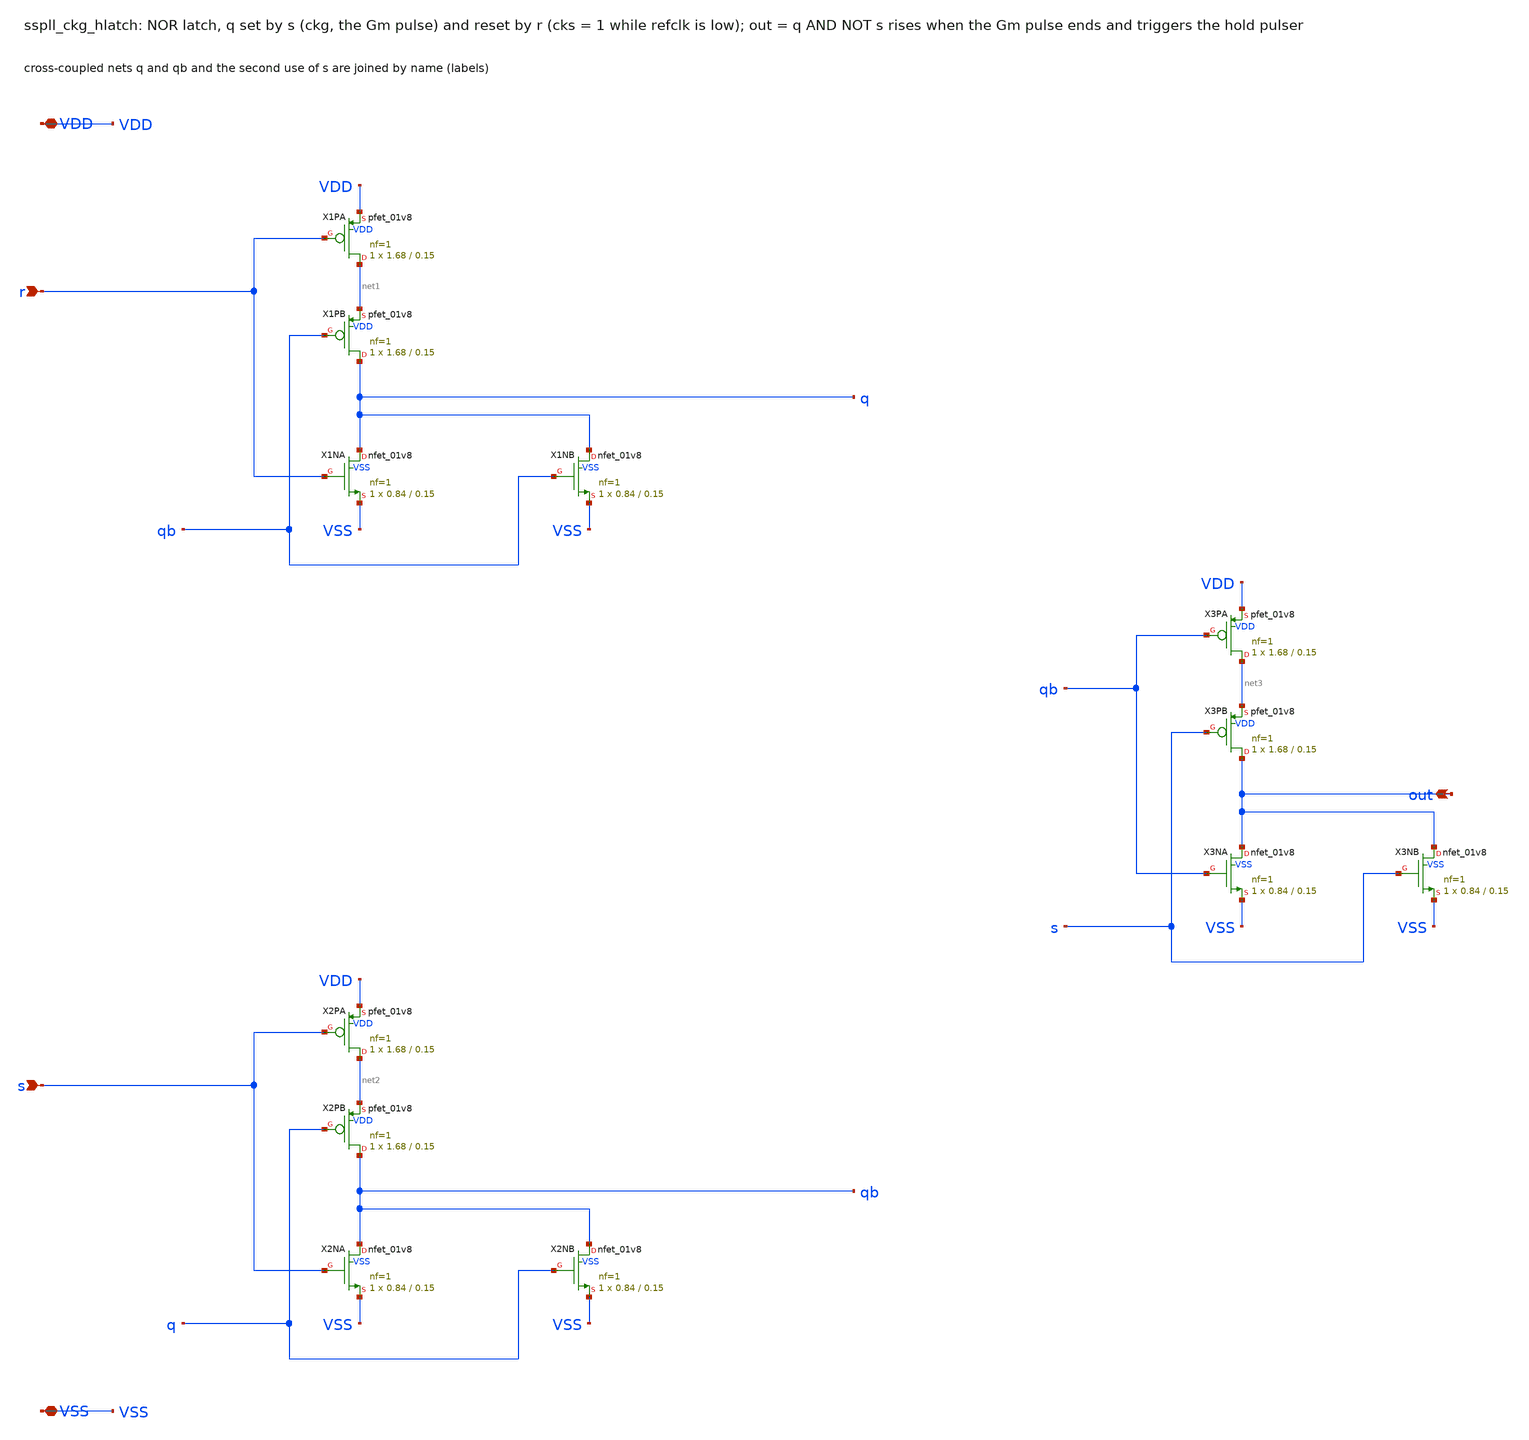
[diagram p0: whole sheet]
** sch_path: xschem/clkgen/sspll_ckg_hlatch.sch
**.subckt sspll_ckg_hlatch r s out VDD VSS
*.ipin r
*.ipin s
*.opin out
*.iopin VDD
*.iopin VSS
XX1PA net1 r VDD VDD sky130_fd_pr__pfet_01v8 L=0.15 W=1.68 nf=1 ad='int((nf+1)/2) * W/nf * 0.29' as='int((nf+2)/2) * W/nf * 0.29'
+ pd='2*int((nf+1)/2) * (W/nf + 0.29)' ps='2*int((nf+2)/2) * (W/nf + 0.29)' nrd='0.29 / W' nrs='0.29 / W'
+ sa=0 sb=0 sd=0 mult=1 m=1
XX1PB q qb net1 VDD sky130_fd_pr__pfet_01v8 L=0.15 W=1.68 nf=1 ad='int((nf+1)/2) * W/nf * 0.29' as='int((nf+2)/2) * W/nf * 0.29'
+ pd='2*int((nf+1)/2) * (W/nf + 0.29)' ps='2*int((nf+2)/2) * (W/nf + 0.29)' nrd='0.29 / W' nrs='0.29 / W'
+ sa=0 sb=0 sd=0 mult=1 m=1
XX1NA q r VSS VSS sky130_fd_pr__nfet_01v8 L=0.15 W=0.84 nf=1 ad='int((nf+1)/2) * W/nf * 0.29' as='int((nf+2)/2) * W/nf * 0.29'
+ pd='2*int((nf+1)/2) * (W/nf + 0.29)' ps='2*int((nf+2)/2) * (W/nf + 0.29)' nrd='0.29 / W' nrs='0.29 / W'
+ sa=0 sb=0 sd=0 mult=1 m=1
XX1NB q qb VSS VSS sky130_fd_pr__nfet_01v8 L=0.15 W=0.84 nf=1 ad='int((nf+1)/2) * W/nf * 0.29' as='int((nf+2)/2) * W/nf * 0.29'
+ pd='2*int((nf+1)/2) * (W/nf + 0.29)' ps='2*int((nf+2)/2) * (W/nf + 0.29)' nrd='0.29 / W' nrs='0.29 / W'
+ sa=0 sb=0 sd=0 mult=1 m=1
XX2PA net2 s VDD VDD sky130_fd_pr__pfet_01v8 L=0.15 W=1.68 nf=1 ad='int((nf+1)/2) * W/nf * 0.29' as='int((nf+2)/2) * W/nf * 0.29'
+ pd='2*int((nf+1)/2) * (W/nf + 0.29)' ps='2*int((nf+2)/2) * (W/nf + 0.29)' nrd='0.29 / W' nrs='0.29 / W'
+ sa=0 sb=0 sd=0 mult=1 m=1
XX2PB qb q net2 VDD sky130_fd_pr__pfet_01v8 L=0.15 W=1.68 nf=1 ad='int((nf+1)/2) * W/nf * 0.29' as='int((nf+2)/2) * W/nf * 0.29'
+ pd='2*int((nf+1)/2) * (W/nf + 0.29)' ps='2*int((nf+2)/2) * (W/nf + 0.29)' nrd='0.29 / W' nrs='0.29 / W'
+ sa=0 sb=0 sd=0 mult=1 m=1
XX2NA qb s VSS VSS sky130_fd_pr__nfet_01v8 L=0.15 W=0.84 nf=1 ad='int((nf+1)/2) * W/nf * 0.29' as='int((nf+2)/2) * W/nf * 0.29'
+ pd='2*int((nf+1)/2) * (W/nf + 0.29)' ps='2*int((nf+2)/2) * (W/nf + 0.29)' nrd='0.29 / W' nrs='0.29 / W'
+ sa=0 sb=0 sd=0 mult=1 m=1
XX2NB qb q VSS VSS sky130_fd_pr__nfet_01v8 L=0.15 W=0.84 nf=1 ad='int((nf+1)/2) * W/nf * 0.29' as='int((nf+2)/2) * W/nf * 0.29'
+ pd='2*int((nf+1)/2) * (W/nf + 0.29)' ps='2*int((nf+2)/2) * (W/nf + 0.29)' nrd='0.29 / W' nrs='0.29 / W'
+ sa=0 sb=0 sd=0 mult=1 m=1
XX3PA net3 qb VDD VDD sky130_fd_pr__pfet_01v8 L=0.15 W=1.68 nf=1 ad='int((nf+1)/2) * W/nf * 0.29' as='int((nf+2)/2) * W/nf * 0.29'
+ pd='2*int((nf+1)/2) * (W/nf + 0.29)' ps='2*int((nf+2)/2) * (W/nf + 0.29)' nrd='0.29 / W' nrs='0.29 / W'
+ sa=0 sb=0 sd=0 mult=1 m=1
XX3PB out s net3 VDD sky130_fd_pr__pfet_01v8 L=0.15 W=1.68 nf=1 ad='int((nf+1)/2) * W/nf * 0.29' as='int((nf+2)/2) * W/nf * 0.29'
+ pd='2*int((nf+1)/2) * (W/nf + 0.29)' ps='2*int((nf+2)/2) * (W/nf + 0.29)' nrd='0.29 / W' nrs='0.29 / W'
+ sa=0 sb=0 sd=0 mult=1 m=1
XX3NA out qb VSS VSS sky130_fd_pr__nfet_01v8 L=0.15 W=0.84 nf=1 ad='int((nf+1)/2) * W/nf * 0.29' as='int((nf+2)/2) * W/nf * 0.29'
+ pd='2*int((nf+1)/2) * (W/nf + 0.29)' ps='2*int((nf+2)/2) * (W/nf + 0.29)' nrd='0.29 / W' nrs='0.29 / W'
+ sa=0 sb=0 sd=0 mult=1 m=1
XX3NB out s VSS VSS sky130_fd_pr__nfet_01v8 L=0.15 W=0.84 nf=1 ad='int((nf+1)/2) * W/nf * 0.29' as='int((nf+2)/2) * W/nf * 0.29'
+ pd='2*int((nf+1)/2) * (W/nf + 0.29)' ps='2*int((nf+2)/2) * (W/nf + 0.29)' nrd='0.29 / W' nrs='0.29 / W'
+ sa=0 sb=0 sd=0 mult=1 m=1
**.ends
.end
